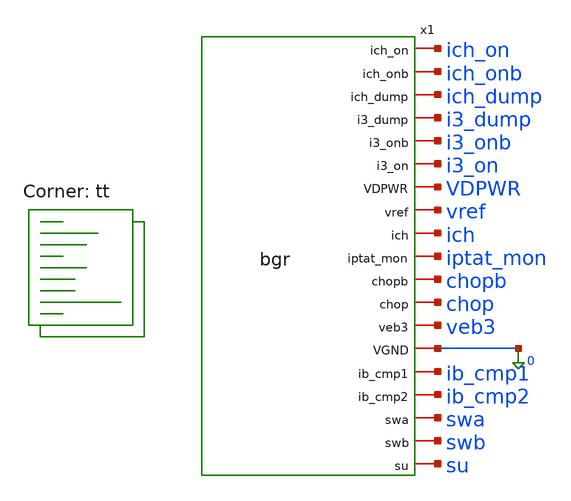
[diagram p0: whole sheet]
** sch_path: xschem/tb_bg_cg.sch
**.subckt tb_bg_cg
x1 ich_on ich_onb ich_dump i3_dump i3_onb i3_on VDPWR vref ich iptat_mon chopb chop veb3 0 ib_cmp1
+ ib_cmp2 swa swb su bgr
**** begin user architecture code
.lib $::SKYWATER_MODELS/sky130.lib.spice tt

Vdd VDPWR 0 1.8
Vswa swa 0 1.8
Vswb swb 0 0
Vchop chop 0 0
Vchopb chopb 0 1.8
Vichon ich_on 0 1.8
Vichonb ich_onb 0 0
Vichdump ich_dump 0 0
Vi3on i3_on 0 1.8
Vi3onb i3_onb 0 0
Vi3dump i3_dump 0 0
* parks as in 3d
E4 p4 0 x1.va 0 1
V4 ich p4 0
V7 iptat_mon p4 0
Vc1 ib_cmp1 0 0.70
Vc2 ib_cmp2 0 0.70
* the design nodeset (step 3)
.nodeset v(x1.vpg)=0.55 v(x1.va)=0.71 v(x1.vb)=0.71 v(vref)=1.25
.control
option temp=25
save all @m.x1.xcore.x1.xmp1.msky130_fd_pr__pfet_01v8[cgg]
+ @m.x1.xcore.x1.xmp2.msky130_fd_pr__pfet_01v8[cgg] @m.x1.xcore.x1.xmp3a.msky130_fd_pr__pfet_01v8[cgg]
+ @m.x1.xcore.x1.xmp3b.msky130_fd_pr__pfet_01v8[cgg] @m.x1.xcore.x1.xmp4a.msky130_fd_pr__pfet_01v8[cgg]
+ @m.x1.xcore.x1.xmp4b.msky130_fd_pr__pfet_01v8[cgg] @m.x1.xcore.x1.xmp7.msky130_fd_pr__pfet_01v8[cgg] @m.x1.xcore.x1.xmp5.msky130_fd_pr__pfet_01v8[cgg]
+ @m.x1.xcore.x1.xmp2.msky130_fd_pr__pfet_01v8[gm] @m.x1.xcore.x1.xmp2.msky130_fd_pr__pfet_01v8[id]
op
let c1 = @m.x1.xcore.x1.xmp1.msky130_fd_pr__pfet_01v8[cgg]*1e12
let c2 = @m.x1.xcore.x1.xmp2.msky130_fd_pr__pfet_01v8[cgg]*1e12
let c3a = @m.x1.xcore.x1.xmp3a.msky130_fd_pr__pfet_01v8[cgg]*1e12
let c3b = @m.x1.xcore.x1.xmp3b.msky130_fd_pr__pfet_01v8[cgg]*1e12
let c4a = @m.x1.xcore.x1.xmp4a.msky130_fd_pr__pfet_01v8[cgg]*1e12
let c4b = @m.x1.xcore.x1.xmp4b.msky130_fd_pr__pfet_01v8[cgg]*1e12
let c7 = @m.x1.xcore.x1.xmp7.msky130_fd_pr__pfet_01v8[cgg]*1e12
let c5 = @m.x1.xcore.x1.xmp5.msky130_fd_pr__pfet_01v8[cgg]*1e12
let csum = c1 + c2 + c3a + c3b + c4a + c4b + c7 + c5
let g2 = @m.x1.xcore.x1.xmp2.msky130_fd_pr__pfet_01v8[gm]*1e6
let i2 = abs(@m.x1.xcore.x1.xmp2.msky130_fd_pr__pfet_01v8[id])*1e9
echo CGG P1=$&c1 P2=$&c2 P3a=$&c3a P3b=$&c3b P4a=$&c4a P4b=$&c4b P7=$&c7 P5=$&c5 sum_pF=$&csum
echo GMP2 gm_uS=$&g2 id_nA=$&i2
.endc

**** end user architecture code
**.ends

* expanding   symbol:  bgr.sym # of pins=19
** sym_path: xschem/bgr.sym
** sch_path: xschem/bgr.sch
.subckt bgr ich_on ich_onb ich_dump i3_dump i3_onb i3_on VDPWR vref ich iptat_mon chopb chop veb3
+ VGND ib_cmp1 ib_cmp2 swa swb su
*.iopin swb
*.iopin VDPWR
*.iopin VGND
*.iopin vref
*.iopin veb3
*.iopin ich
*.iopin iptat_mon
*.iopin ib_cmp1
*.iopin ib_cmp2
*.iopin swa
*.iopin chop
*.iopin chopb
*.iopin ich_on
*.iopin ich_onb
*.iopin ich_dump
*.iopin i3_on
*.iopin i3_onb
*.iopin i3_dump
*.iopin su
xcore vpg VDPWR i3b vref ichb ich vb iptat_mon veb3 VGND va ibias ib_cmp1 ib_cmp2 su bg_core
xota inp inn vpg VDPWR VGND ibias chop chopb ota2s
XS1 va swa inn VGND sky130_fd_pr__nfet_01v8_lvt L=0.5 W=4 nf=1 ad='int((1 + 1)/2) * 4 / 1 * 0.29' as='int((1 + 2)/2) * 4 / 1 * 0.29'
+ pd='2*int((1 + 1)/2) * (4 / 1 + 0.29)' ps='2*int((1 + 2)/2) * (4 / 1 + 0.29)' nrd='0.29 / 4 ' nrs='0.29 / 4 '
+ sa=0 sb=0 sd=0 mult=1 m=1
XS2 vb swa inp VGND sky130_fd_pr__nfet_01v8_lvt L=0.5 W=4 nf=1 ad='int((1 + 1)/2) * 4 / 1 * 0.29' as='int((1 + 2)/2) * 4 / 1 * 0.29'
+ pd='2*int((1 + 1)/2) * (4 / 1 + 0.29)' ps='2*int((1 + 2)/2) * (4 / 1 + 0.29)' nrd='0.29 / 4 ' nrs='0.29 / 4 '
+ sa=0 sb=0 sd=0 mult=1 m=1
XS3 va swb inp VGND sky130_fd_pr__nfet_01v8_lvt L=0.5 W=4 nf=1 ad='int((1 + 1)/2) * 4 / 1 * 0.29' as='int((1 + 2)/2) * 4 / 1 * 0.29'
+ pd='2*int((1 + 1)/2) * (4 / 1 + 0.29)' ps='2*int((1 + 2)/2) * (4 / 1 + 0.29)' nrd='0.29 / 4 ' nrs='0.29 / 4 '
+ sa=0 sb=0 sd=0 mult=1 m=1
XS4 vb swb inn VGND sky130_fd_pr__nfet_01v8_lvt L=0.5 W=4 nf=1 ad='int((1 + 1)/2) * 4 / 1 * 0.29' as='int((1 + 2)/2) * 4 / 1 * 0.29'
+ pd='2*int((1 + 1)/2) * (4 / 1 + 0.29)' ps='2*int((1 + 2)/2) * (4 / 1 + 0.29)' nrd='0.29 / 4 ' nrs='0.29 / 4 '
+ sa=0 sb=0 sd=0 mult=1 m=1
XS_ichon_n ichb ich_on ich VGND sky130_fd_pr__nfet_01v8 L=0.5 W=2 nf=1 ad='int((1 + 1)/2) * 2 / 1 * 0.29'
+ as='int((1 + 2)/2) * 2 / 1 * 0.29' pd='2*int((1 + 1)/2) * (2 / 1 + 0.29)' ps='2*int((1 + 2)/2) * (2 / 1 + 0.29)'
+ nrd='0.29 / 2 ' nrs='0.29 / 2 ' sa=0 sb=0 sd=0 mult=1 m=1
XS_ichon_p ichb ich_onb ich VDPWR sky130_fd_pr__pfet_01v8 L=0.5 W=4 nf=1 ad='int((1 + 1)/2) * 4 / 1 * 0.29'
+ as='int((1 + 2)/2) * 4 / 1 * 0.29' pd='2*int((1 + 1)/2) * (4 / 1 + 0.29)' ps='2*int((1 + 2)/2) * (4 / 1 + 0.29)'
+ nrd='0.29 / 4 ' nrs='0.29 / 4 ' sa=0 sb=0 sd=0 mult=1 m=1
XS_ichdump ichb ich_dump VGND VGND sky130_fd_pr__nfet_01v8 L=0.5 W=1 nf=1 ad='int((1 + 1)/2) * 1 / 1 * 0.29'
+ as='int((1 + 2)/2) * 1 / 1 * 0.29' pd='2*int((1 + 1)/2) * (1 / 1 + 0.29)' ps='2*int((1 + 2)/2) * (1 / 1 + 0.29)'
+ nrd='0.29 / 1 ' nrs='0.29 / 1 ' sa=0 sb=0 sd=0 mult=1 m=1
XS_i3on_n i3b i3_on vref VGND sky130_fd_pr__nfet_01v8 L=0.5 W=2 nf=1 ad='int((1 + 1)/2) * 2 / 1 * 0.29'
+ as='int((1 + 2)/2) * 2 / 1 * 0.29' pd='2*int((1 + 1)/2) * (2 / 1 + 0.29)' ps='2*int((1 + 2)/2) * (2 / 1 + 0.29)'
+ nrd='0.29 / 2 ' nrs='0.29 / 2 ' sa=0 sb=0 sd=0 mult=1 m=1
XS_i3on_p i3b i3_onb vref VDPWR sky130_fd_pr__pfet_01v8 L=0.5 W=4 nf=1 ad='int((1 + 1)/2) * 4 / 1 * 0.29'
+ as='int((1 + 2)/2) * 4 / 1 * 0.29' pd='2*int((1 + 1)/2) * (4 / 1 + 0.29)' ps='2*int((1 + 2)/2) * (4 / 1 + 0.29)'
+ nrd='0.29 / 4 ' nrs='0.29 / 4 ' sa=0 sb=0 sd=0 mult=1 m=1
XS_i3dump i3b i3_dump VGND VGND sky130_fd_pr__nfet_01v8 L=0.5 W=1 nf=1 ad='int((1 + 1)/2) * 1 / 1 * 0.29'
+ as='int((1 + 2)/2) * 1 / 1 * 0.29' pd='2*int((1 + 1)/2) * (1 / 1 + 0.29)' ps='2*int((1 + 2)/2) * (1 / 1 + 0.29)'
+ nrd='0.29 / 1 ' nrs='0.29 / 1 ' sa=0 sb=0 sd=0 mult=1 m=1
.ends


* expanding   symbol:  bg_core.sym # of pins=15
** sym_path: xschem/bg_core.sym
** sch_path: xschem/bg_core.sch
.subckt bg_core vpg VDPWR i3b vref ichb ich vb iptat_mon veb3 VGND va ibias ib_cmp1 ib_cmp2 su
*.iopin va
*.iopin vb
*.iopin vref
*.iopin veb3
*.iopin vpg
*.iopin i3b
*.iopin VDPWR
*.iopin ichb
*.iopin ich
*.iopin iptat_mon
*.iopin ibias
*.iopin ib_cmp1
*.iopin ib_cmp2
*.iopin VGND
*.iopin su
x1 vpg VDPWR i3b vref ichb ich vb iptat_mon nb va bg_mirror
x2 vb vref veb3 VGND eb2 bg_rrow
x3 va veb3 eb2 VGND bg_pnp
XMNB1 nb nb VGND VGND sky130_fd_pr__nfet_01v8 L=8 W=4 nf=1 ad='int((1 + 1)/2) * 4 / 1 * 0.29' as='int((1 + 2)/2) * 4 / 1 * 0.29'
+ pd='2*int((1 + 1)/2) * (4 / 1 + 0.29)' ps='2*int((1 + 2)/2) * (4 / 1 + 0.29)' nrd='0.29 / 4 ' nrs='0.29 / 4 '
+ sa=0 sb=0 sd=0 mult=1 m=1
XMNB2 ibias nb VGND VGND sky130_fd_pr__nfet_01v8 L=8 W=4 nf=1 ad='int((1 + 1)/2) * 4 / 1 * 0.29' as='int((1 + 2)/2) * 4 / 1 * 0.29'
+ pd='2*int((1 + 1)/2) * (4 / 1 + 0.29)' ps='2*int((1 + 2)/2) * (4 / 1 + 0.29)' nrd='0.29 / 4 ' nrs='0.29 / 4 '
+ sa=0 sb=0 sd=0 mult=1 m=1
XMNB3 ib_cmp1 nb VGND VGND sky130_fd_pr__nfet_01v8 L=8 W=4 nf=1 ad='int((1 + 1)/2) * 4 / 1 * 0.29' as='int((1 + 2)/2) * 4 / 1 * 0.29'
+ pd='2*int((1 + 1)/2) * (4 / 1 + 0.29)' ps='2*int((1 + 2)/2) * (4 / 1 + 0.29)' nrd='0.29 / 4 ' nrs='0.29 / 4 '
+ sa=0 sb=0 sd=0 mult=4 m=4
XMNB4 ib_cmp2 nb VGND VGND sky130_fd_pr__nfet_01v8 L=8 W=4 nf=1 ad='int((1 + 1)/2) * 4 / 1 * 0.29' as='int((1 + 2)/2) * 4 / 1 * 0.29'
+ pd='2*int((1 + 1)/2) * (4 / 1 + 0.29)' ps='2*int((1 + 2)/2) * (4 / 1 + 0.29)' nrd='0.29 / 4 ' nrs='0.29 / 4 '
+ sa=0 sb=0 sd=0 mult=4 m=4
xsu VDPWR vref vpg su VGND nb bg_su
.ends


* expanding   symbol:  ota2s.sym # of pins=8
** sym_path: xschem/ota2s.sym
** sch_path: xschem/ota2s.sch
.subckt ota2s INP INN OUT VDPWR VGND IBIAS CHOP CHOPB
*.ipin INN
*.ipin INP
*.ipin IBIAS
*.opin OUT
*.iopin VDPWR
*.iopin VGND
*.ipin CHOPB
*.ipin CHOP
XMREF IBIAS IBIAS VDPWR VDPWR sky130_fd_pr__pfet_01v8 L=4 W=20 nf=1 ad='int((1 + 1)/2) * 20 / 1 * 0.29'
+ as='int((1 + 2)/2) * 20 / 1 * 0.29' pd='2*int((1 + 1)/2) * (20 / 1 + 0.29)' ps='2*int((1 + 2)/2) * (20 / 1 + 0.29)'
+ nrd='0.29 / 20 ' nrs='0.29 / 20 ' sa=0 sb=0 sd=0 mult=1 m=1
XMTAIL tail IBIAS VDPWR VDPWR sky130_fd_pr__pfet_01v8 L=4 W=20 nf=1 ad='int((1 + 1)/2) * 20 / 1 * 0.29'
+ as='int((1 + 2)/2) * 20 / 1 * 0.29' pd='2*int((1 + 1)/2) * (20 / 1 + 0.29)' ps='2*int((1 + 2)/2) * (20 / 1 + 0.29)'
+ nrd='0.29 / 20 ' nrs='0.29 / 20 ' sa=0 sb=0 sd=0 mult=2 m=2
XMP1 d1 INN tail VDPWR sky130_fd_pr__pfet_01v8_lvt L=6 W=25 nf=1 ad='int((1 + 1)/2) * 25 / 1 * 0.29'
+ as='int((1 + 2)/2) * 25 / 1 * 0.29' pd='2*int((1 + 1)/2) * (25 / 1 + 0.29)' ps='2*int((1 + 2)/2) * (25 / 1 + 0.29)'
+ nrd='0.29 / 25 ' nrs='0.29 / 25 ' sa=0 sb=0 sd=0 mult=24 m=24
XMP2 x1 INP tail VDPWR sky130_fd_pr__pfet_01v8_lvt L=6 W=25 nf=1 ad='int((1 + 1)/2) * 25 / 1 * 0.29'
+ as='int((1 + 2)/2) * 25 / 1 * 0.29' pd='2*int((1 + 1)/2) * (25 / 1 + 0.29)' ps='2*int((1 + 2)/2) * (25 / 1 + 0.29)'
+ nrd='0.29 / 25 ' nrs='0.29 / 25 ' sa=0 sb=0 sd=0 mult=24 m=24
XMN1 d1 g12 VGND VGND sky130_fd_pr__nfet_01v8 L=20 W=6 nf=1 ad='int((1 + 1)/2) * 6 / 1 * 0.29' as='int((1 + 2)/2) * 6 / 1 * 0.29'
+ pd='2*int((1 + 1)/2) * (6 / 1 + 0.29)' ps='2*int((1 + 2)/2) * (6 / 1 + 0.29)' nrd='0.29 / 6 ' nrs='0.29 / 6 '
+ sa=0 sb=0 sd=0 mult=2 m=2
XMN2 x1 g12 VGND VGND sky130_fd_pr__nfet_01v8 L=20 W=6 nf=1 ad='int((1 + 1)/2) * 6 / 1 * 0.29' as='int((1 + 2)/2) * 6 / 1 * 0.29'
+ pd='2*int((1 + 1)/2) * (6 / 1 + 0.29)' ps='2*int((1 + 2)/2) * (6 / 1 + 0.29)' nrd='0.29 / 6 ' nrs='0.29 / 6 '
+ sa=0 sb=0 sd=0 mult=2 m=2
XMP3 OUT IBIAS VDPWR VDPWR sky130_fd_pr__pfet_01v8 L=4 W=20 nf=1 ad='int((1 + 1)/2) * 20 / 1 * 0.29'
+ as='int((1 + 2)/2) * 20 / 1 * 0.29' pd='2*int((1 + 1)/2) * (20 / 1 + 0.29)' ps='2*int((1 + 2)/2) * (20 / 1 + 0.29)'
+ nrd='0.29 / 20 ' nrs='0.29 / 20 ' sa=0 sb=0 sd=0 mult=6 m=6
XMN3 OUT g3 VGND VGND sky130_fd_pr__nfet_01v8 L=1 W=7 nf=1 ad='int((1 + 1)/2) * 7 / 1 * 0.29' as='int((1 + 2)/2) * 7 / 1 * 0.29'
+ pd='2*int((1 + 1)/2) * (7 / 1 + 0.29)' ps='2*int((1 + 2)/2) * (7 / 1 + 0.29)' nrd='0.29 / 7 ' nrs='0.29 / 7 '
+ sa=0 sb=0 sd=0 mult=1 m=1
XRZ1 net1 g3 VGND sky130_fd_pr__res_high_po_1p41 L=20 mult=1 m=1
XRZ2 net2 net1 VGND sky130_fd_pr__res_high_po_1p41 L=20 mult=1 m=1
XRZ3 net3 net2 VGND sky130_fd_pr__res_high_po_1p41 L=20 mult=1 m=1
XRZ4 net4 net3 VGND sky130_fd_pr__res_high_po_1p41 L=20 mult=1 m=1
XRZ5 net5 net4 VGND sky130_fd_pr__res_high_po_1p41 L=20 mult=1 m=1
XRZ6 cz net5 VGND sky130_fd_pr__res_high_po_1p41 L=20 mult=1 m=1
XCC cz OUT sky130_fd_pr__cap_mim_m3_1 W=25 L=25 MF=8 m=8
XDP tail VDPWR tail VDPWR sky130_fd_pr__pfet_01v8_lvt L=6 W=25 nf=1 ad='int((1 + 1)/2) * 25 / 1 * 0.29'
+ as='int((1 + 2)/2) * 25 / 1 * 0.29' pd='2*int((1 + 1)/2) * (25 / 1 + 0.29)' ps='2*int((1 + 2)/2) * (25 / 1 + 0.29)'
+ nrd='0.29 / 25 ' nrs='0.29 / 25 ' sa=0 sb=0 sd=0 mult=8 m=8
XDNA d1 VGND VGND VGND sky130_fd_pr__nfet_01v8 L=20 W=6 nf=1 ad='int((1 + 1)/2) * 6 / 1 * 0.29' as='int((1 + 2)/2) * 6 / 1 * 0.29'
+ pd='2*int((1 + 1)/2) * (6 / 1 + 0.29)' ps='2*int((1 + 2)/2) * (6 / 1 + 0.29)' nrd='0.29 / 6 ' nrs='0.29 / 6 '
+ sa=0 sb=0 sd=0 mult=2 m=2
XDNB x1 VGND VGND VGND sky130_fd_pr__nfet_01v8 L=20 W=6 nf=1 ad='int((1 + 1)/2) * 6 / 1 * 0.29' as='int((1 + 2)/2) * 6 / 1 * 0.29'
+ pd='2*int((1 + 1)/2) * (6 / 1 + 0.29)' ps='2*int((1 + 2)/2) * (6 / 1 + 0.29)' nrd='0.29 / 6 ' nrs='0.29 / 6 '
+ sa=0 sb=0 sd=0 mult=2 m=2
XDB VDPWR VDPWR VDPWR VDPWR sky130_fd_pr__pfet_01v8 L=4 W=20 nf=1 ad='int((1 + 1)/2) * 20 / 1 * 0.29'
+ as='int((1 + 2)/2) * 20 / 1 * 0.29' pd='2*int((1 + 1)/2) * (20 / 1 + 0.29)' ps='2*int((1 + 2)/2) * (20 / 1 + 0.29)'
+ nrd='0.29 / 20 ' nrs='0.29 / 20 ' sa=0 sb=0 sd=0 mult=2 m=2
XRD1 VGND VGND VGND sky130_fd_pr__res_high_po_1p41 L=20 mult=1 m=1
XRD2 VGND VGND VGND sky130_fd_pr__res_high_po_1p41 L=20 mult=1 m=1
XSD1 d1 CHOPB g12 VGND sky130_fd_pr__nfet_01v8 L=0.5 W=6 nf=1 ad='int((1 + 1)/2) * 6 / 1 * 0.29' as='int((1 + 2)/2) * 6 / 1 * 0.29'
+ pd='2*int((1 + 1)/2) * (6 / 1 + 0.29)' ps='2*int((1 + 2)/2) * (6 / 1 + 0.29)' nrd='0.29 / 6 ' nrs='0.29 / 6 '
+ sa=0 sb=0 sd=0 mult=1 m=1
XSD2 x1 CHOP g12 VGND sky130_fd_pr__nfet_01v8 L=0.5 W=6 nf=1 ad='int((1 + 1)/2) * 6 / 1 * 0.29' as='int((1 + 2)/2) * 6 / 1 * 0.29'
+ pd='2*int((1 + 1)/2) * (6 / 1 + 0.29)' ps='2*int((1 + 2)/2) * (6 / 1 + 0.29)' nrd='0.29 / 6 ' nrs='0.29 / 6 '
+ sa=0 sb=0 sd=0 mult=1 m=1
XSG2 g3 CHOP d1 VGND sky130_fd_pr__nfet_01v8 L=0.5 W=6 nf=1 ad='int((1 + 1)/2) * 6 / 1 * 0.29' as='int((1 + 2)/2) * 6 / 1 * 0.29'
+ pd='2*int((1 + 1)/2) * (6 / 1 + 0.29)' ps='2*int((1 + 2)/2) * (6 / 1 + 0.29)' nrd='0.29 / 6 ' nrs='0.29 / 6 '
+ sa=0 sb=0 sd=0 mult=1 m=1
XSG1 x1 CHOPB g3 VGND sky130_fd_pr__nfet_01v8 L=0.5 W=6 nf=1 ad='int((1 + 1)/2) * 6 / 1 * 0.29' as='int((1 + 2)/2) * 6 / 1 * 0.29'
+ pd='2*int((1 + 1)/2) * (6 / 1 + 0.29)' ps='2*int((1 + 2)/2) * (6 / 1 + 0.29)' nrd='0.29 / 6 ' nrs='0.29 / 6 '
+ sa=0 sb=0 sd=0 mult=1 m=1
.ends


* expanding   symbol:  bg_mirror.sym # of pins=10
** sym_path: xschem/bg_mirror.sym
** sch_path: xschem/bg_mirror.sch
.subckt bg_mirror vpg VDPWR d3b d3a d4b d4a d2 d7 d5 d1
*.iopin vpg
*.iopin VDPWR
*.iopin d1
*.iopin d2
*.iopin d3a
*.iopin d3b
*.iopin d4a
*.iopin d4b
*.iopin d7
*.iopin d5
XMP1 d1 vpg VDPWR VDPWR sky130_fd_pr__pfet_01v8 L=20 W=8.8 nf=1 ad='int((1 + 1)/2) * 8.8 / 1 * 0.29'
+ as='int((1 + 2)/2) * 8.8 / 1 * 0.29' pd='2*int((1 + 1)/2) * (8.8 / 1 + 0.29)' ps='2*int((1 + 2)/2) * (8.8 / 1 + 0.29)'
+ nrd='0.29 / 8.8 ' nrs='0.29 / 8.8 ' sa=0 sb=0 sd=0 mult=4 m=4
XMP2 d2 vpg VDPWR VDPWR sky130_fd_pr__pfet_01v8 L=20 W=8.8 nf=1 ad='int((1 + 1)/2) * 8.8 / 1 * 0.29'
+ as='int((1 + 2)/2) * 8.8 / 1 * 0.29' pd='2*int((1 + 1)/2) * (8.8 / 1 + 0.29)' ps='2*int((1 + 2)/2) * (8.8 / 1 + 0.29)'
+ nrd='0.29 / 8.8 ' nrs='0.29 / 8.8 ' sa=0 sb=0 sd=0 mult=4 m=4
XMP3A d3a vpg VDPWR VDPWR sky130_fd_pr__pfet_01v8 L=20 W=8.8 nf=1 ad='int((1 + 1)/2) * 8.8 / 1 * 0.29'
+ as='int((1 + 2)/2) * 8.8 / 1 * 0.29' pd='2*int((1 + 1)/2) * (8.8 / 1 + 0.29)' ps='2*int((1 + 2)/2) * (8.8 / 1 + 0.29)'
+ nrd='0.29 / 8.8 ' nrs='0.29 / 8.8 ' sa=0 sb=0 sd=0 mult=2 m=2
XMP3B d3b vpg VDPWR VDPWR sky130_fd_pr__pfet_01v8 L=20 W=8.8 nf=1 ad='int((1 + 1)/2) * 8.8 / 1 * 0.29'
+ as='int((1 + 2)/2) * 8.8 / 1 * 0.29' pd='2*int((1 + 1)/2) * (8.8 / 1 + 0.29)' ps='2*int((1 + 2)/2) * (8.8 / 1 + 0.29)'
+ nrd='0.29 / 8.8 ' nrs='0.29 / 8.8 ' sa=0 sb=0 sd=0 mult=2 m=2
XMP4A d4a vpg VDPWR VDPWR sky130_fd_pr__pfet_01v8 L=20 W=8.8 nf=1 ad='int((1 + 1)/2) * 8.8 / 1 * 0.29'
+ as='int((1 + 2)/2) * 8.8 / 1 * 0.29' pd='2*int((1 + 1)/2) * (8.8 / 1 + 0.29)' ps='2*int((1 + 2)/2) * (8.8 / 1 + 0.29)'
+ nrd='0.29 / 8.8 ' nrs='0.29 / 8.8 ' sa=0 sb=0 sd=0 mult=1 m=1
XMP4B d4b vpg VDPWR VDPWR sky130_fd_pr__pfet_01v8 L=20 W=8.8 nf=1 ad='int((1 + 1)/2) * 8.8 / 1 * 0.29'
+ as='int((1 + 2)/2) * 8.8 / 1 * 0.29' pd='2*int((1 + 1)/2) * (8.8 / 1 + 0.29)' ps='2*int((1 + 2)/2) * (8.8 / 1 + 0.29)'
+ nrd='0.29 / 8.8 ' nrs='0.29 / 8.8 ' sa=0 sb=0 sd=0 mult=1 m=1
XMP7 d7 vpg VDPWR VDPWR sky130_fd_pr__pfet_01v8 L=20 W=8.8 nf=1 ad='int((1 + 1)/2) * 8.8 / 1 * 0.29'
+ as='int((1 + 2)/2) * 8.8 / 1 * 0.29' pd='2*int((1 + 1)/2) * (8.8 / 1 + 0.29)' ps='2*int((1 + 2)/2) * (8.8 / 1 + 0.29)'
+ nrd='0.29 / 8.8 ' nrs='0.29 / 8.8 ' sa=0 sb=0 sd=0 mult=2 m=2
XMP5 d5 vpg VDPWR VDPWR sky130_fd_pr__pfet_01v8 L=20 W=8.8 nf=1 ad='int((1 + 1)/2) * 8.8 / 1 * 0.29'
+ as='int((1 + 2)/2) * 8.8 / 1 * 0.29' pd='2*int((1 + 1)/2) * (8.8 / 1 + 0.29)' ps='2*int((1 + 2)/2) * (8.8 / 1 + 0.29)'
+ nrd='0.29 / 8.8 ' nrs='0.29 / 8.8 ' sa=0 sb=0 sd=0 mult=2 m=2
.ends


* expanding   symbol:  bg_rrow.sym # of pins=5
** sym_path: xschem/bg_rrow.sym
** sch_path: xschem/bg_rrow.sch
.subckt bg_rrow vb vref veb3 VGND eb2
*.iopin vb
*.iopin eb2
*.iopin vref
*.iopin veb3
*.iopin VGND
XR1_1 eb2 net1 VGND sky130_fd_pr__res_high_po_1p41 L=20 mult=1 m=1
XR1_2 net1 net2 VGND sky130_fd_pr__res_high_po_1p41 L=20 mult=1 m=1
XR1_3 net2 net3 VGND sky130_fd_pr__res_high_po_1p41 L=20 mult=1 m=1
XR1_4 net3 vb VGND sky130_fd_pr__res_high_po_1p41 L=20 mult=1 m=1
XR3[39] r3n[38] vref VGND sky130_fd_pr__res_high_po_1p41 L=20 mult=1 m=1
XR3[38] r3n[37] r3n[38] VGND sky130_fd_pr__res_high_po_1p41 L=20 mult=1 m=1
XR3[37] r3n[36] r3n[37] VGND sky130_fd_pr__res_high_po_1p41 L=20 mult=1 m=1
XR3[36] r3n[35] r3n[36] VGND sky130_fd_pr__res_high_po_1p41 L=20 mult=1 m=1
XR3[35] r3n[34] r3n[35] VGND sky130_fd_pr__res_high_po_1p41 L=20 mult=1 m=1
XR3[34] r3n[33] r3n[34] VGND sky130_fd_pr__res_high_po_1p41 L=20 mult=1 m=1
XR3[33] r3n[32] r3n[33] VGND sky130_fd_pr__res_high_po_1p41 L=20 mult=1 m=1
XR3[32] r3n[31] r3n[32] VGND sky130_fd_pr__res_high_po_1p41 L=20 mult=1 m=1
XR3[31] r3n[30] r3n[31] VGND sky130_fd_pr__res_high_po_1p41 L=20 mult=1 m=1
XR3[30] r3n[29] r3n[30] VGND sky130_fd_pr__res_high_po_1p41 L=20 mult=1 m=1
XR3[29] r3n[28] r3n[29] VGND sky130_fd_pr__res_high_po_1p41 L=20 mult=1 m=1
XR3[28] r3n[27] r3n[28] VGND sky130_fd_pr__res_high_po_1p41 L=20 mult=1 m=1
XR3[27] r3n[26] r3n[27] VGND sky130_fd_pr__res_high_po_1p41 L=20 mult=1 m=1
XR3[26] r3n[25] r3n[26] VGND sky130_fd_pr__res_high_po_1p41 L=20 mult=1 m=1
XR3[25] r3n[24] r3n[25] VGND sky130_fd_pr__res_high_po_1p41 L=20 mult=1 m=1
XR3[24] r3n[23] r3n[24] VGND sky130_fd_pr__res_high_po_1p41 L=20 mult=1 m=1
XR3[23] r3n[22] r3n[23] VGND sky130_fd_pr__res_high_po_1p41 L=20 mult=1 m=1
XR3[22] r3n[21] r3n[22] VGND sky130_fd_pr__res_high_po_1p41 L=20 mult=1 m=1
XR3[21] r3n[20] r3n[21] VGND sky130_fd_pr__res_high_po_1p41 L=20 mult=1 m=1
XR3[20] r3n[19] r3n[20] VGND sky130_fd_pr__res_high_po_1p41 L=20 mult=1 m=1
XR3[19] r3n[18] r3n[19] VGND sky130_fd_pr__res_high_po_1p41 L=20 mult=1 m=1
XR3[18] r3n[17] r3n[18] VGND sky130_fd_pr__res_high_po_1p41 L=20 mult=1 m=1
XR3[17] r3n[16] r3n[17] VGND sky130_fd_pr__res_high_po_1p41 L=20 mult=1 m=1
XR3[16] r3n[15] r3n[16] VGND sky130_fd_pr__res_high_po_1p41 L=20 mult=1 m=1
XR3[15] r3n[14] r3n[15] VGND sky130_fd_pr__res_high_po_1p41 L=20 mult=1 m=1
XR3[14] r3n[13] r3n[14] VGND sky130_fd_pr__res_high_po_1p41 L=20 mult=1 m=1
XR3[13] r3n[12] r3n[13] VGND sky130_fd_pr__res_high_po_1p41 L=20 mult=1 m=1
XR3[12] r3n[11] r3n[12] VGND sky130_fd_pr__res_high_po_1p41 L=20 mult=1 m=1
XR3[11] r3n[10] r3n[11] VGND sky130_fd_pr__res_high_po_1p41 L=20 mult=1 m=1
XR3[10] r3n[9] r3n[10] VGND sky130_fd_pr__res_high_po_1p41 L=20 mult=1 m=1
XR3[9] r3n[8] r3n[9] VGND sky130_fd_pr__res_high_po_1p41 L=20 mult=1 m=1
XR3[8] r3n[7] r3n[8] VGND sky130_fd_pr__res_high_po_1p41 L=20 mult=1 m=1
XR3[7] r3n[6] r3n[7] VGND sky130_fd_pr__res_high_po_1p41 L=20 mult=1 m=1
XR3[6] r3n[5] r3n[6] VGND sky130_fd_pr__res_high_po_1p41 L=20 mult=1 m=1
XR3[5] r3n[4] r3n[5] VGND sky130_fd_pr__res_high_po_1p41 L=20 mult=1 m=1
XR3[4] r3n[3] r3n[4] VGND sky130_fd_pr__res_high_po_1p41 L=20 mult=1 m=1
XR3[3] r3n[2] r3n[3] VGND sky130_fd_pr__res_high_po_1p41 L=20 mult=1 m=1
XR3[2] r3n[1] r3n[2] VGND sky130_fd_pr__res_high_po_1p41 L=20 mult=1 m=1
XR3[1] r3n[0] r3n[1] VGND sky130_fd_pr__res_high_po_1p41 L=20 mult=1 m=1
XR3[0] veb3 r3n[0] VGND sky130_fd_pr__res_high_po_1p41 L=20 mult=1 m=1
XRD[3] VGND VGND VGND sky130_fd_pr__res_high_po_1p41 L=20 mult=1 m=1
XRD[2] VGND VGND VGND sky130_fd_pr__res_high_po_1p41 L=20 mult=1 m=1
XRD[1] VGND VGND VGND sky130_fd_pr__res_high_po_1p41 L=20 mult=1 m=1
XRD[0] VGND VGND VGND sky130_fd_pr__res_high_po_1p41 L=20 mult=1 m=1
.ends


* expanding   symbol:  bg_pnp.sym # of pins=4
** sym_path: xschem/bg_pnp.sym
** sch_path: xschem/bg_pnp.sch
.subckt bg_pnp va veb3 eb2 VGND
*.iopin va
*.iopin eb2
*.iopin veb3
*.iopin VGND
XQ1 VGND VGND va sky130_fd_pr__pnp_05v5_W3p40L3p40 m=1
XQ2 VGND VGND eb2 sky130_fd_pr__pnp_05v5_W3p40L3p40 m=8
XQ3 VGND VGND veb3 sky130_fd_pr__pnp_05v5_W3p40L3p40 m=1
XQD VGND VGND VGND sky130_fd_pr__pnp_05v5_W3p40L3p40 m=15
.ends


* expanding   symbol:  bg_su.sym # of pins=6
** sym_path: xschem/bg_su.sym
** sch_path: xschem/bg_su.sch
.subckt bg_su VDPWR vref vpg su VGND nb
*.iopin vref
*.iopin VGND
*.iopin vpg
*.iopin VDPWR
*.iopin su
*.iopin nb
XMSU1 su vref VDPWR VDPWR sky130_fd_pr__pfet_01v8 L=20 W=0.42 nf=1 ad='int((1 + 1)/2) * 0.42 / 1 * 0.29'
+ as='int((1 + 2)/2) * 0.42 / 1 * 0.29' pd='2*int((1 + 1)/2) * (0.42 / 1 + 0.29)' ps='2*int((1 + 2)/2) * (0.42 / 1 + 0.29)'
+ nrd='0.29 / 0.42 ' nrs='0.29 / 0.42 ' sa=0 sb=0 sd=0 mult=1 m=1
XMSU3 su nb VGND VGND sky130_fd_pr__nfet_01v8 L=1 W=0.42 nf=1 ad='int((1 + 1)/2) * 0.42 / 1 * 0.29' as='int((1 + 2)/2) * 0.42 / 1 * 0.29'
+ pd='2*int((1 + 1)/2) * (0.42 / 1 + 0.29)' ps='2*int((1 + 2)/2) * (0.42 / 1 + 0.29)' nrd='0.29 / 0.42 '
+ nrs='0.29 / 0.42 ' sa=0 sb=0 sd=0 mult=1 m=1
XMSU2 vpg su VGND VGND sky130_fd_pr__nfet_01v8 L=10 W=0.42 nf=1 ad='int((1 + 1)/2) * 0.42 / 1 * 0.29'
+ as='int((1 + 2)/2) * 0.42 / 1 * 0.29' pd='2*int((1 + 1)/2) * (0.42 / 1 + 0.29)' ps='2*int((1 + 2)/2) * (0.42 / 1 + 0.29)'
+ nrd='0.29 / 0.42 ' nrs='0.29 / 0.42 ' sa=0 sb=0 sd=0 mult=1 m=1
.ends

.end
